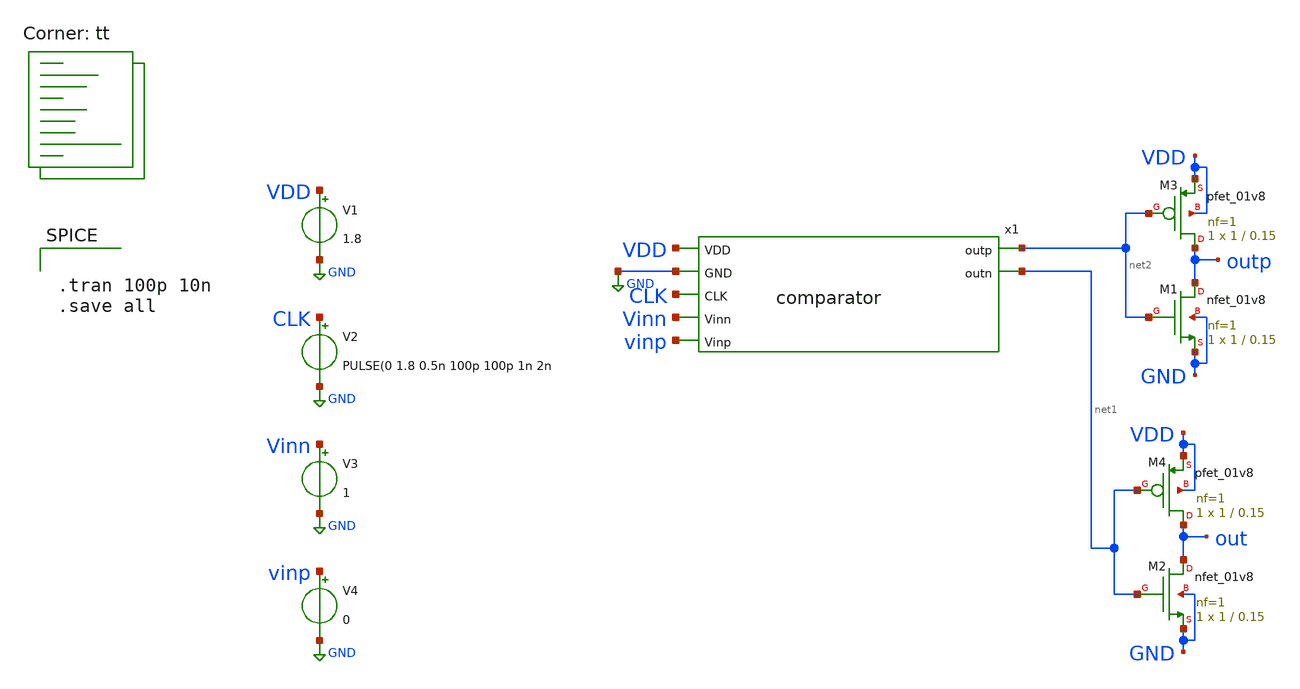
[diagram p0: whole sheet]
** sch_path: xschem/vault/comparator test.sch
**.subckt comparator test
x1 VDD GND CLK net2 net1 Vinn vinp comparator
V2 CLK GND PULSE(0 1.8 0.5n 100p 100p 1n 2n
V1 VDD GND 1.8
V3 Vinn GND 1
V4 vinp GND 0
XM1 outp net2 GND GND sky130_fd_pr__nfet_01v8 L=0.15 W=1 nf=1 ad='int((nf+1)/2) * W/nf * 0.29' as='int((nf+2)/2) * W/nf * 0.29'
+ pd='2*int((nf+1)/2) * (W/nf + 0.29)' ps='2*int((nf+2)/2) * (W/nf + 0.29)' nrd='0.29 / W' nrs='0.29 / W'
+ sa=0 sb=0 sd=0 mult=1 m=1
XM2 out net1 GND GND sky130_fd_pr__nfet_01v8 L=0.15 W=1 nf=1 ad='int((nf+1)/2) * W/nf * 0.29' as='int((nf+2)/2) * W/nf * 0.29'
+ pd='2*int((nf+1)/2) * (W/nf + 0.29)' ps='2*int((nf+2)/2) * (W/nf + 0.29)' nrd='0.29 / W' nrs='0.29 / W'
+ sa=0 sb=0 sd=0 mult=1 m=1
XM3 outp net2 VDD VDD sky130_fd_pr__pfet_01v8 L=0.15 W=1 nf=1 ad='int((nf+1)/2) * W/nf * 0.29' as='int((nf+2)/2) * W/nf * 0.29'
+ pd='2*int((nf+1)/2) * (W/nf + 0.29)' ps='2*int((nf+2)/2) * (W/nf + 0.29)' nrd='0.29 / W' nrs='0.29 / W'
+ sa=0 sb=0 sd=0 mult=1 m=1
XM4 out net1 VDD VDD sky130_fd_pr__pfet_01v8 L=0.15 W=1 nf=1 ad='int((nf+1)/2) * W/nf * 0.29' as='int((nf+2)/2) * W/nf * 0.29'
+ pd='2*int((nf+1)/2) * (W/nf + 0.29)' ps='2*int((nf+2)/2) * (W/nf + 0.29)' nrd='0.29 / W' nrs='0.29 / W'
+ sa=0 sb=0 sd=0 mult=1 m=1
**** begin user architecture code
.lib $::SKYWATER_MODELS/sky130.lib.spice tt


.tran 100p 10n
.save all


**** end user architecture code
**.ends
.GLOBAL GND
.end
